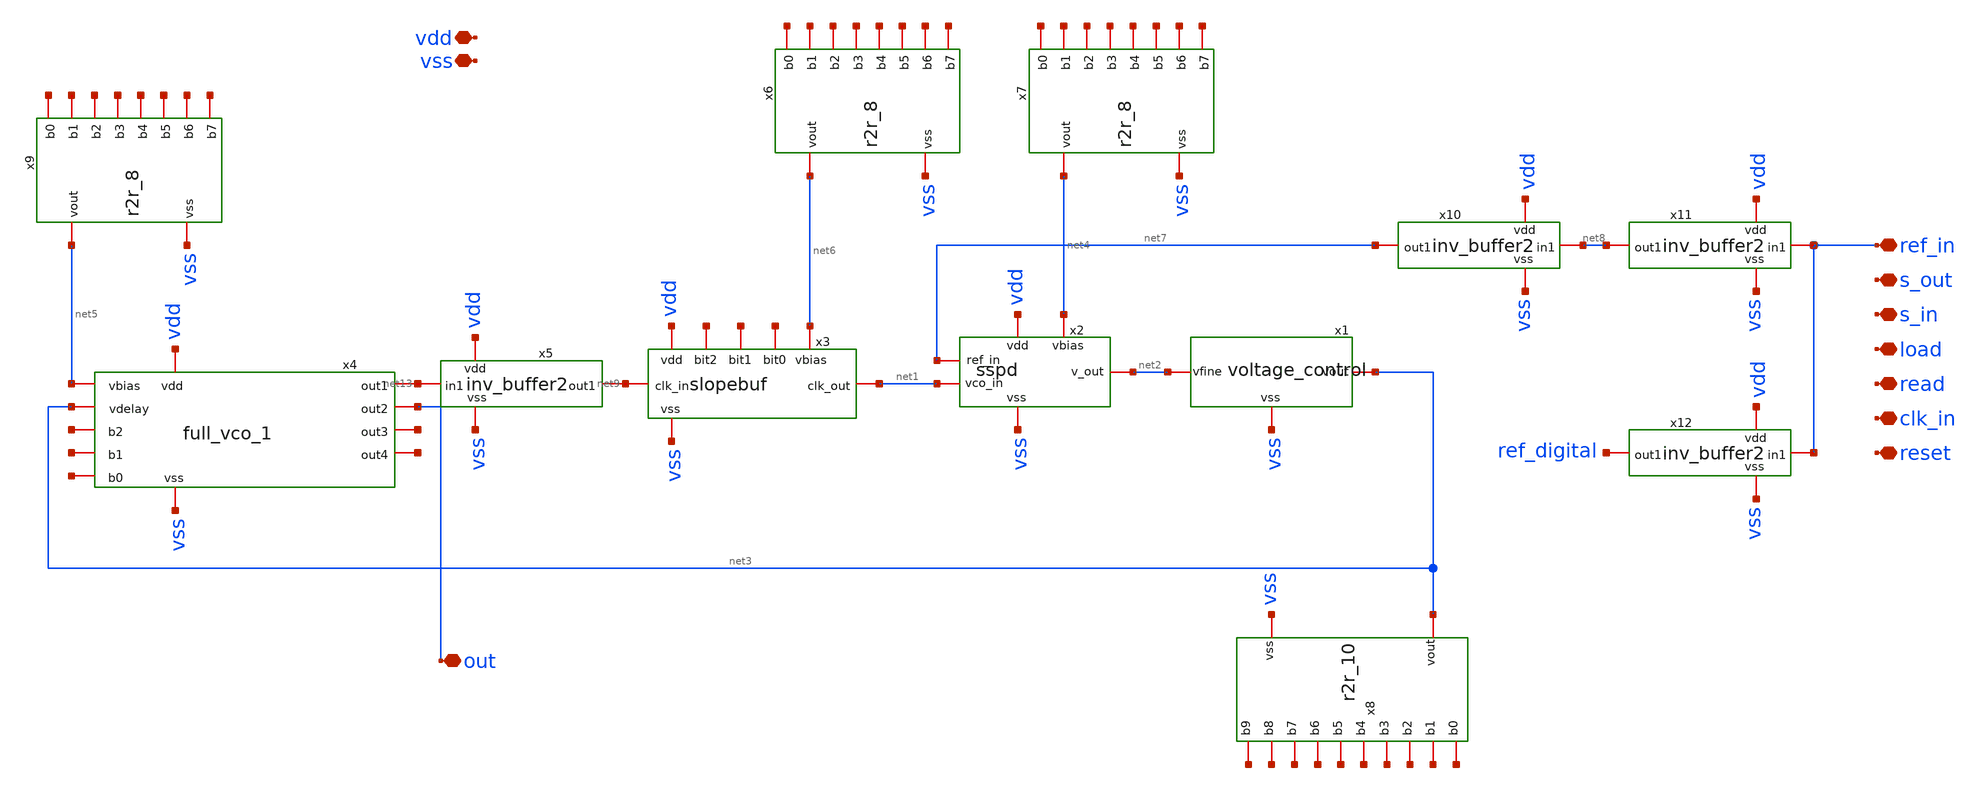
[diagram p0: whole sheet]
** sch_path: xschem/full_IC_1.sch
**.subckt full_IC_1 vdd vss ref_in s_in load read clk_in reset s_out out
*.iopin vdd
*.iopin vss
*.iopin ref_in
*.iopin s_in
*.iopin load
*.iopin read
*.iopin clk_in
*.iopin reset
*.iopin s_out
*.iopin out
x1 vss net2 net3 voltage_control
x2 vdd vss net7 net1 net4 net2 sspd
x3 vdd vss net9 net1 net10 net11 net12 net6 slopebuf
x4 net13 vdd vss out net5 net3 net14 net15 net16 net17 net18 full_vco_1
x5 vdd vss net9 net13 inv_buffer2
x7 net4 net19 net20 net21 vss net22 net23 net24 net25 net26 r2r_8
x8 net3 net27 net28 net29 net30 net31 net32 net33 net34 net35 vss net36 r2r_10
x9 net5 net37 net38 net39 vss net40 net41 net42 net43 net44 r2r_8
x6 net6 net45 net46 net47 vss net48 net49 net50 net51 net52 r2r_8
x10 vdd vss net7 net8 inv_buffer2
x11 vdd vss net8 ref_in inv_buffer2
x12 vdd vss ref_digital ref_in inv_buffer2
**.ends
.end
